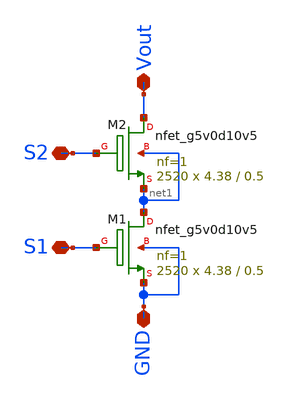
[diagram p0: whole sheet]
** sch_path: mag/lvs_test/nwaffle_x2.sch
**.subckt nwaffle_x2 Vout GND S1 S2
*.iopin Vout
*.iopin GND
*.iopin S1
*.iopin S2
XM1 net1 S1 GND GND sky130_fd_pr__nfet_g5v0d10v5 L=0.5 W=4.38 nf=1 ad='int((nf+1)/2) * W/nf * 0.29' as='int((nf+2)/2) * W/nf * 0.29'
+ pd='2*int((nf+1)/2) * (W/nf + 0.29)' ps='2*int((nf+2)/2) * (W/nf + 0.29)' nrd='0.29 / W' nrs='0.29 / W'
+ sa=0 sb=0 sd=0 mult=2520 m=2520
XM2 Vout S2 net1 net1 sky130_fd_pr__nfet_g5v0d10v5 L=0.5 W=4.38 nf=1 ad='int((nf+1)/2) * W/nf * 0.29'
+ as='int((nf+2)/2) * W/nf * 0.29' pd='2*int((nf+1)/2) * (W/nf + 0.29)' ps='2*int((nf+2)/2) * (W/nf + 0.29)'
+ nrd='0.29 / W' nrs='0.29 / W' sa=0 sb=0 sd=0 mult=2520 m=2520
**.ends
.end
